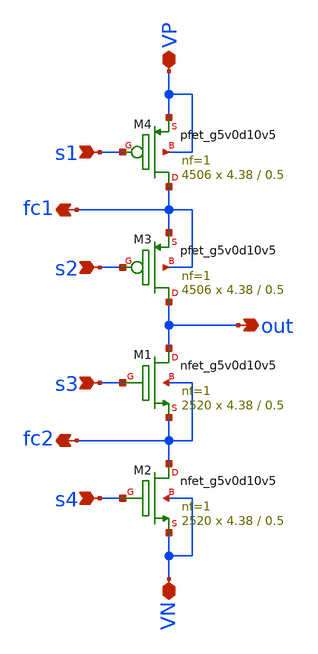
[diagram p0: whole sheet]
** sch_path: xschem/hierarchy_sch/power_stage.sch
**.subckt power_stage s1 s2 s3 s4 VP VN out fc1 fc2
*.ipin s1
*.ipin s2
*.ipin s3
*.ipin s4
*.iopin VP
*.iopin VN
*.opin out
*.opin fc1
*.opin fc2
XM1 out s3 fc2 fc2 sky130_fd_pr__nfet_g5v0d10v5 L=0.5 W=4.38 nf=1 ad='int((nf+1)/2) * W/nf * 0.29' as='int((nf+2)/2) * W/nf * 0.29'
+ pd='2*int((nf+1)/2) * (W/nf + 0.29)' ps='2*int((nf+2)/2) * (W/nf + 0.29)' nrd='0.29 / W' nrs='0.29 / W'
+ sa=0 sb=0 sd=0 mult=2520 m=2520
XM2 fc2 s4 VN VN sky130_fd_pr__nfet_g5v0d10v5 L=0.5 W=4.38 nf=1 ad='int((nf+1)/2) * W/nf * 0.29' as='int((nf+2)/2) * W/nf * 0.29'
+ pd='2*int((nf+1)/2) * (W/nf + 0.29)' ps='2*int((nf+2)/2) * (W/nf + 0.29)' nrd='0.29 / W' nrs='0.29 / W'
+ sa=0 sb=0 sd=0 mult=2520 m=2520
XM3 out s2 fc1 fc1 sky130_fd_pr__pfet_g5v0d10v5 L=0.5 W=4.38 nf=1 ad='int((nf+1)/2) * W/nf * 0.29' as='int((nf+2)/2) * W/nf * 0.29'
+ pd='2*int((nf+1)/2) * (W/nf + 0.29)' ps='2*int((nf+2)/2) * (W/nf + 0.29)' nrd='0.29 / W' nrs='0.29 / W'
+ sa=0 sb=0 sd=0 mult=4506 m=4506
XM4 fc1 s1 VP VP sky130_fd_pr__pfet_g5v0d10v5 L=0.5 W=4.38 nf=1 ad='int((nf+1)/2) * W/nf * 0.29' as='int((nf+2)/2) * W/nf * 0.29'
+ pd='2*int((nf+1)/2) * (W/nf + 0.29)' ps='2*int((nf+2)/2) * (W/nf + 0.29)' nrd='0.29 / W' nrs='0.29 / W'
+ sa=0 sb=0 sd=0 mult=4506 m=4506
**.ends
.end
